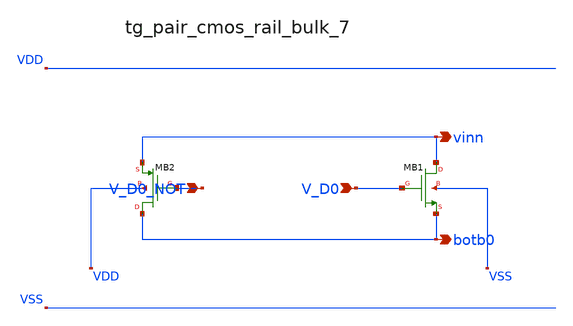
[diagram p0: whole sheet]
** sch_path: analog-db/raw/ia_005_hsu_pga_ideal/hier/blocks/tg_pair_cmos_rail_bulk_7.sch
**.subckt tg_pair_cmos_rail_bulk_7 V_D0_NOT V_D0 vinn botb0
*.ipin V_D0_NOT
*.ipin V_D0
*.opin vinn
*.opin botb0
XMB1 vinn V_D0 botb0 VSS sg13_lv_nmos w=x_dut_xmb1_w l=x_dut_xmb1_l ng=1 m=x_dut_xmb1_m
XMB2 botb0 V_D0_NOT vinn VDD sg13_lv_pmos w=x_dut_xmb2_w l=x_dut_xmb2_l ng=1 m=x_dut_xmb2_m
**.ends
.end
